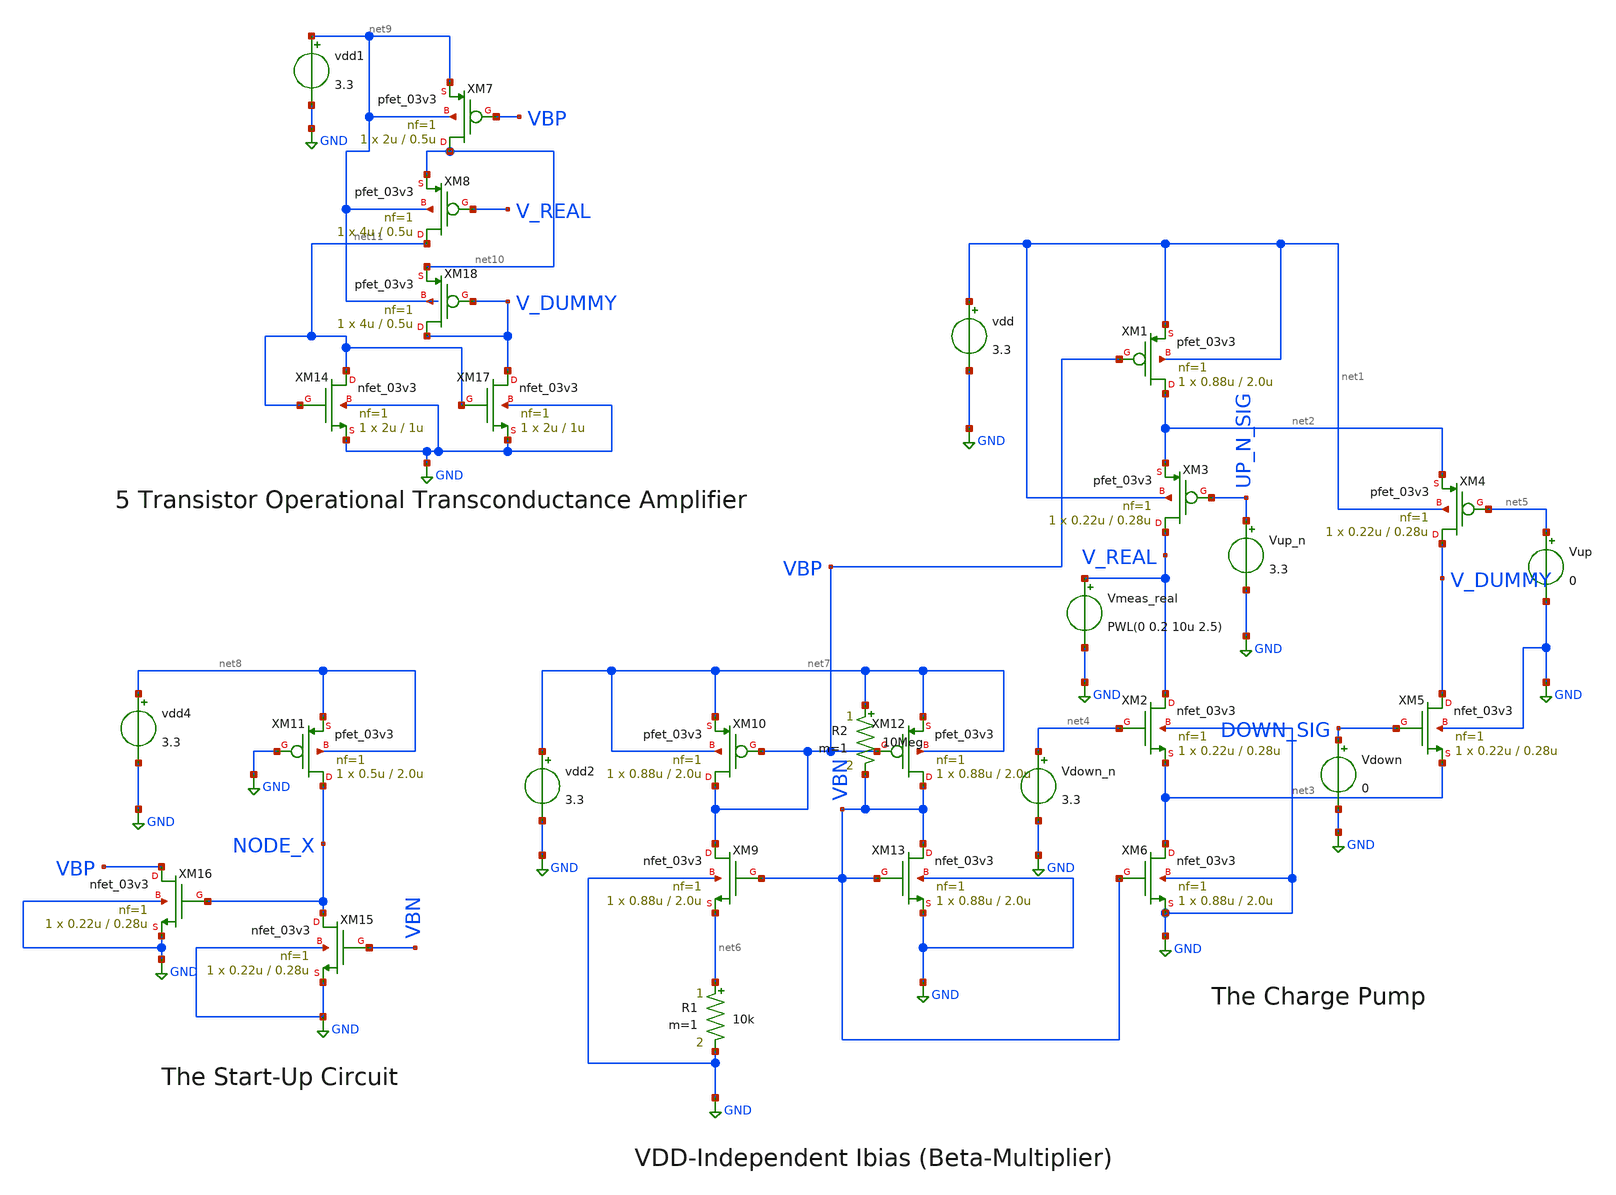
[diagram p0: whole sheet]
** sch_path: src/ChargePump/cp_amp.sch
* Copyright 2022 GlobalFoundries PDK Authors
* Licensed under the Apache License, Version 2.0 (the "License");
* you may not use this file except in compliance with the License.
* You may obtain a copy of the License at
* https://www.apache.org/licenses/LICENSE-2.0
* Unless required by applicable law or agreed to in writing, software
* distributed under the License is distributed on an "AS IS" BASIS,
* WITHOUT WARRANTIES OR CONDITIONS OF ANY KIND, either express or implied.
* See the License for the specific language governing permissions and
* limitations under the License.
**.subckt cp_amp
XM1 net2 VBP net1 net1 pfet_03v3 L=2.0u W=0.88u nf=1 ad='int((nf+1)/2) * W/nf * 0.18u' as='int((nf+2)/2) * W/nf * 0.18u'
+ pd='2*int((nf+1)/2) * (W/nf + 0.18u)' ps='2*int((nf+2)/2) * (W/nf + 0.18u)' nrd='0.18u / W' nrs='0.18u / W'
+ sa=0 sb=0 sd=0 m=1
XM2 V_REAL net4 net3 GND nfet_03v3 L=0.28u W=0.22u nf=1 ad='int((nf+1)/2) * W/nf * 0.18u' as='int((nf+2)/2) * W/nf * 0.18u'
+ pd='2*int((nf+1)/2) * (W/nf + 0.18u)' ps='2*int((nf+2)/2) * (W/nf + 0.18u)' nrd='0.18u / W' nrs='0.18u / W'
+ sa=0 sb=0 sd=0 m=1
vdd net1 GND 3.3
XM3 V_REAL UP_N_SIG net2 net1 pfet_03v3 L=0.28u W=0.22u nf=1 ad='int((nf+1)/2) * W/nf * 0.18u' as='int((nf+2)/2) * W/nf * 0.18u'
+ pd='2*int((nf+1)/2) * (W/nf + 0.18u)' ps='2*int((nf+2)/2) * (W/nf + 0.18u)' nrd='0.18u / W' nrs='0.18u / W'
+ sa=0 sb=0 sd=0 m=1
XM4 V_DUMMY net5 net2 net1 pfet_03v3 L=0.28u W=0.22u nf=1 ad='int((nf+1)/2) * W/nf * 0.18u' as='int((nf+2)/2) * W/nf * 0.18u'
+ pd='2*int((nf+1)/2) * (W/nf + 0.18u)' ps='2*int((nf+2)/2) * (W/nf + 0.18u)' nrd='0.18u / W' nrs='0.18u / W'
+ sa=0 sb=0 sd=0 m=1
XM5 V_DUMMY DOWN_SIG net3 GND nfet_03v3 L=0.28u W=0.22u nf=1 ad='int((nf+1)/2) * W/nf * 0.18u' as='int((nf+2)/2) * W/nf * 0.18u'
+ pd='2*int((nf+1)/2) * (W/nf + 0.18u)' ps='2*int((nf+2)/2) * (W/nf + 0.18u)' nrd='0.18u / W' nrs='0.18u / W'
+ sa=0 sb=0 sd=0 m=1
XM6 net3 VBN GND GND nfet_03v3 L=2.0u W=0.88u nf=1 ad='int((nf+1)/2) * W/nf * 0.18u' as='int((nf+2)/2) * W/nf * 0.18u'
+ pd='2*int((nf+1)/2) * (W/nf + 0.18u)' ps='2*int((nf+2)/2) * (W/nf + 0.18u)' nrd='0.18u / W' nrs='0.18u / W'
+ sa=0 sb=0 sd=0 m=1
Vdown DOWN_SIG GND 0
Vup net5 GND 0
Vup_n UP_N_SIG GND 3.3
Vdown_n net4 GND 3.3
vdd2 net7 GND 3.3
XM10 VBP VBP net7 net7 pfet_03v3 L=2.0u W=0.88u nf=1 ad='int((nf+1)/2) * W/nf * 0.18u' as='int((nf+2)/2) * W/nf * 0.18u'
+ pd='2*int((nf+1)/2) * (W/nf + 0.18u)' ps='2*int((nf+2)/2) * (W/nf + 0.18u)' nrd='0.18u / W' nrs='0.18u / W'
+ sa=0 sb=0 sd=0 m=1
XM9 VBP VBN net6 GND nfet_03v3 L=2.0u W=0.88u nf=1 ad='int((nf+1)/2) * W/nf * 0.18u' as='int((nf+2)/2) * W/nf * 0.18u'
+ pd='2*int((nf+1)/2) * (W/nf + 0.18u)' ps='2*int((nf+2)/2) * (W/nf + 0.18u)' nrd='0.18u / W' nrs='0.18u / W'
+ sa=0 sb=0 sd=0 m=1
R1 net6 GND 10k m=1
XM12 VBN VBP net7 net7 pfet_03v3 L=2.0u W=0.88u nf=1 ad='int((nf+1)/2) * W/nf * 0.18u' as='int((nf+2)/2) * W/nf * 0.18u'
+ pd='2*int((nf+1)/2) * (W/nf + 0.18u)' ps='2*int((nf+2)/2) * (W/nf + 0.18u)' nrd='0.18u / W' nrs='0.18u / W'
+ sa=0 sb=0 sd=0 m=1
XM13 VBN VBN GND GND nfet_03v3 L=2.0u W=0.88u nf=1 ad='int((nf+1)/2) * W/nf * 0.18u' as='int((nf+2)/2) * W/nf * 0.18u'
+ pd='2*int((nf+1)/2) * (W/nf + 0.18u)' ps='2*int((nf+2)/2) * (W/nf + 0.18u)' nrd='0.18u / W' nrs='0.18u / W'
+ sa=0 sb=0 sd=0 m=1
XM11 NODE_X GND net8 net8 pfet_03v3 L=2.0u W=0.5u nf=1 ad='int((nf+1)/2) * W/nf * 0.18u' as='int((nf+2)/2) * W/nf * 0.18u'
+ pd='2*int((nf+1)/2) * (W/nf + 0.18u)' ps='2*int((nf+2)/2) * (W/nf + 0.18u)' nrd='0.18u / W' nrs='0.18u / W'
+ sa=0 sb=0 sd=0 m=1
vdd4 net8 GND 3.3
XM15 NODE_X VBN GND GND nfet_03v3 L=0.28u W=0.22u nf=1 ad='int((nf+1)/2) * W/nf * 0.18u' as='int((nf+2)/2) * W/nf * 0.18u'
+ pd='2*int((nf+1)/2) * (W/nf + 0.18u)' ps='2*int((nf+2)/2) * (W/nf + 0.18u)' nrd='0.18u / W' nrs='0.18u / W'
+ sa=0 sb=0 sd=0 m=1
XM16 VBP NODE_X GND GND nfet_03v3 L=0.28u W=0.22u nf=1 ad='int((nf+1)/2) * W/nf * 0.18u' as='int((nf+2)/2) * W/nf * 0.18u'
+ pd='2*int((nf+1)/2) * (W/nf + 0.18u)' ps='2*int((nf+2)/2) * (W/nf + 0.18u)' nrd='0.18u / W' nrs='0.18u / W'
+ sa=0 sb=0 sd=0 m=1
Vmeas_real V_REAL GND PWL(0 0.2 10u 2.5)
XM7 net10 VBP net9 net9 pfet_03v3 L=0.5u W=2u nf=1 ad='int((nf+1)/2) * W/nf * 0.18u' as='int((nf+2)/2) * W/nf * 0.18u'
+ pd='2*int((nf+1)/2) * (W/nf + 0.18u)' ps='2*int((nf+2)/2) * (W/nf + 0.18u)' nrd='0.18u / W' nrs='0.18u / W'
+ sa=0 sb=0 sd=0 m=1
vdd1 net9 GND 3.3
XM14 net11 net11 GND GND nfet_03v3 L=1u W=2u nf=1 ad='int((nf+1)/2) * W/nf * 0.18u' as='int((nf+2)/2) * W/nf * 0.18u'
+ pd='2*int((nf+1)/2) * (W/nf + 0.18u)' ps='2*int((nf+2)/2) * (W/nf + 0.18u)' nrd='0.18u / W' nrs='0.18u / W'
+ sa=0 sb=0 sd=0 m=1
XM8 net11 V_REAL net10 net9 pfet_03v3 L=0.5u W=4u nf=1 ad='int((nf+1)/2) * W/nf * 0.18u' as='int((nf+2)/2) * W/nf * 0.18u'
+ pd='2*int((nf+1)/2) * (W/nf + 0.18u)' ps='2*int((nf+2)/2) * (W/nf + 0.18u)' nrd='0.18u / W' nrs='0.18u / W'
+ sa=0 sb=0 sd=0 m=1
XM18 V_DUMMY V_DUMMY net10 net9 pfet_03v3 L=0.5u W=4u nf=1 ad='int((nf+1)/2) * W/nf * 0.18u' as='int((nf+2)/2) * W/nf * 0.18u'
+ pd='2*int((nf+1)/2) * (W/nf + 0.18u)' ps='2*int((nf+2)/2) * (W/nf + 0.18u)' nrd='0.18u / W' nrs='0.18u / W'
+ sa=0 sb=0 sd=0 m=1
XM17 V_DUMMY net11 GND GND nfet_03v3 L=1u W=2u nf=1 ad='int((nf+1)/2) * W/nf * 0.18u' as='int((nf+2)/2) * W/nf * 0.18u'
+ pd='2*int((nf+1)/2) * (W/nf + 0.18u)' ps='2*int((nf+2)/2) * (W/nf + 0.18u)' nrd='0.18u / W' nrs='0.18u / W'
+ sa=0 sb=0 sd=0 m=1
R2 net7 VBN 10Meg m=1
**** begin user architecture code

* Include global parameters
.include /foss/pdks/gf180mcuD/libs.tech/ngspice/design.ngspice

*Include the GF180MCU models
.lib /foss/pdks/gf180mcuD/libs.tech/ngspice/sm141064.ngspice typical
.nodeset v(vbn)=0.8 v(vbp)=0.6
.control
* MEASURE UP CURRENT

alter Vup_n 0
alter Vup 3.3

alter Vdown_n 0
alter Vdown 3.3

* Run 10us transient to sweep the PWL source
tran 10n 10u
let i_up = -Vmeas_real#branch
let v_out = v(V_REAL)

* MEASURE DOWN CURRENT
alter Vup_n 3.3
alter Vup 0
alter Vdown_n 3.3
alter Vdown 0

* Run the second transient sweep
tran 10n 10u
let i_down = Vmeas_real#branch

* MATH & PLOTTING
setplot tran2
let mismatch = ((abs(tran1.i_up) - abs(i_down)) / abs(tran1.i_up)) * 100

* Plot the currents against the PWL Voltage
plot tran1.i_up i_down vs tran1.v_out title 'Current Matching vs Voltage'

* Plot the mismatch error percentage
plot mismatch vs tran1.v_out title 'Mismatch (%)' ylabel '%' xlabel 'Vout (V)'

* Save to local directory
wrdata /foss/designs/ChargePump/cp_mismatch.txt tran1.v_out tran1.i_up i_down mismatch
.endc

**** end user architecture code
**.ends
.GLOBAL GND
.end
